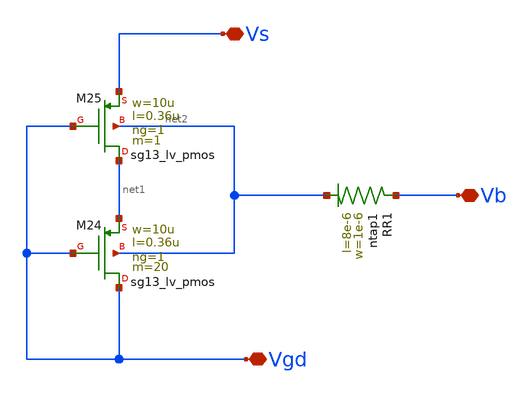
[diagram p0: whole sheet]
** sch_path: Layouts/ib_ctat_ptat/untitled-14.sch
**.subckt untitled-14 Vs Vb Vgd
*.iopin Vs
*.iopin Vb
*.iopin Vgd
XM24 Vgd Vgd net1 net2 sg13_lv_pmos w=10u l=0.36u ng=1 m=20 mm_ok=1
XM25 net1 Vgd Vs net2 sg13_lv_pmos w=10u l=0.36u ng=1 m=1 mm_ok=1
XR1 Vb net2 ntap1 R=37.69 w=1e-6 l=8e-6
**.ends
.end
